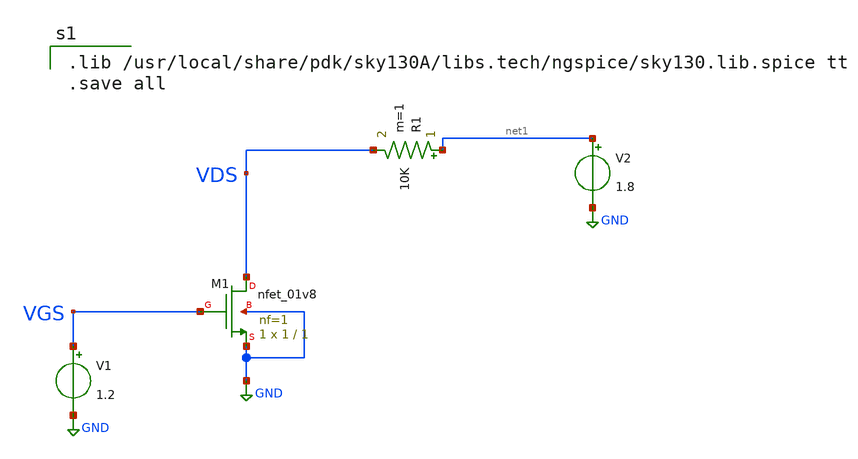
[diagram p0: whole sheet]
** sch_path: MOSFET_Current_Source/NMOS_Current_source.sch
**.subckt NMOS_Current_source
XM1 VDS VGS GND GND sky130_fd_pr__nfet_01v8 L=1 W=1 nf=1 ad='int((1 + 1)/2) * 1 / 1 * 0.29' as='int((1 + 2)/2) * 1 / 1 * 0.29'
+ pd='2*int((1 + 1)/2) * (1 / 1 + 0.29)' ps='2*int((1 + 2)/2) * (1 / 1 + 0.29)' nrd='0.29 / 1 ' nrs='0.29 / 1 '
+ sa=0 sb=0 sd=0 mult=1 m=1
V1 VGS GND 1.2
V2 net1 GND 1.8
R1 net1 VDS 10K m=1
**** begin user architecture code

.lib /usr/local/share/pdk/sky130A/libs.tech/ngspice/sky130.lib.spice tt
.save all


**** end user architecture code
**.ends
.GLOBAL GND
.end
